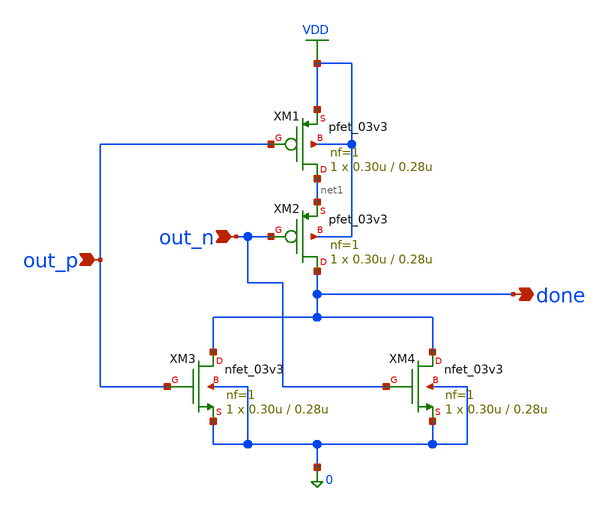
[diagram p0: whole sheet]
** sch_path: xschem/sar_adc/blocks/async_sar/completion_detector.sch
**.subckt completion_detector out_p out_n done
*.ipin out_p
*.ipin out_n
*.opin done
XM1 net1 out_p VDD VDD pfet_03v3 L=0.28u W=0.30u nf=1 ad='int((nf+1)/2) * W/nf * 0.18u' as='int((nf+2)/2) * W/nf * 0.18u'
+ pd='2*int((nf+1)/2) * (W/nf + 0.18u)' ps='2*int((nf+2)/2) * (W/nf + 0.18u)' nrd='0.18u / W' nrs='0.18u / W'
+ sa=0 sb=0 sd=0 m=1
XM2 done out_n net1 VDD pfet_03v3 L=0.28u W=0.30u nf=1 ad='int((nf+1)/2) * W/nf * 0.18u' as='int((nf+2)/2) * W/nf * 0.18u'
+ pd='2*int((nf+1)/2) * (W/nf + 0.18u)' ps='2*int((nf+2)/2) * (W/nf + 0.18u)' nrd='0.18u / W' nrs='0.18u / W'
+ sa=0 sb=0 sd=0 m=1
XM3 done out_p 0 0 nfet_03v3 L=0.28u W=0.30u nf=1 ad='int((nf+1)/2) * W/nf * 0.18u' as='int((nf+2)/2) * W/nf * 0.18u'
+ pd='2*int((nf+1)/2) * (W/nf + 0.18u)' ps='2*int((nf+2)/2) * (W/nf + 0.18u)' nrd='0.18u / W' nrs='0.18u / W'
+ sa=0 sb=0 sd=0 m=1
XM4 done out_n 0 0 nfet_03v3 L=0.28u W=0.30u nf=1 ad='int((nf+1)/2) * W/nf * 0.18u' as='int((nf+2)/2) * W/nf * 0.18u'
+ pd='2*int((nf+1)/2) * (W/nf + 0.18u)' ps='2*int((nf+2)/2) * (W/nf + 0.18u)' nrd='0.18u / W' nrs='0.18u / W'
+ sa=0 sb=0 sd=0 m=1
**.ends
.GLOBAL VDD
.end
